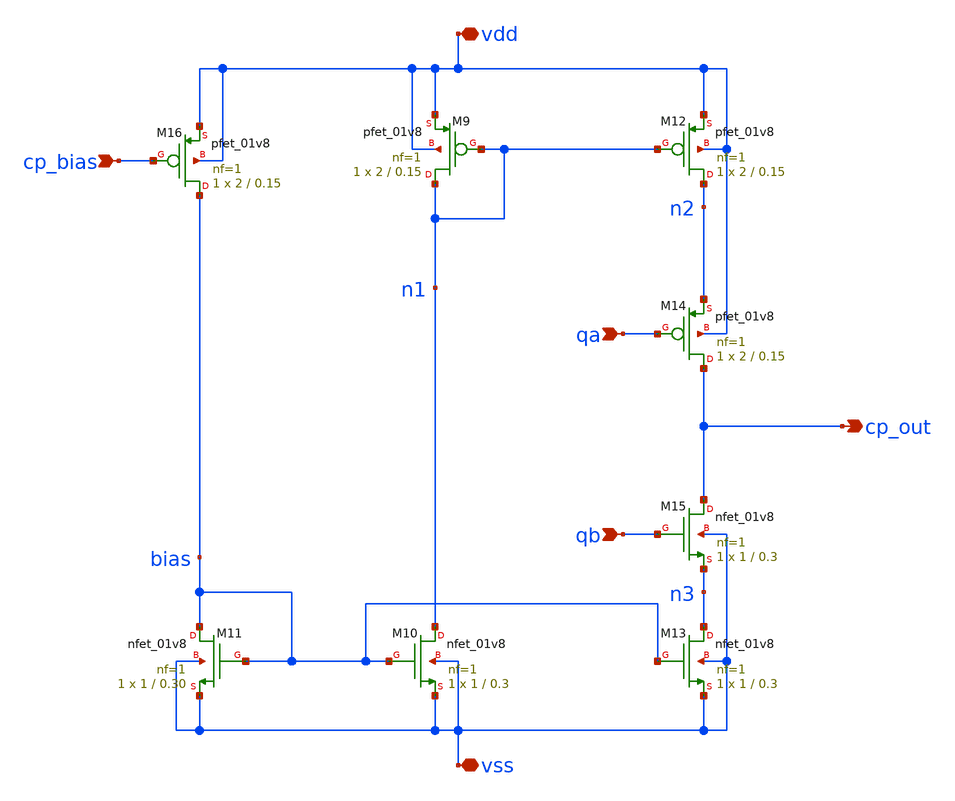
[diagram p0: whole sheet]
** sch_path: xschem/cp/cp_layout.sch
**.subckt cp_layout qa qb cp_out vdd vss cp_bias
*.ipin qa
*.ipin qb
*.opin cp_out
*.iopin vdd
*.iopin vss
*.ipin cp_bias
XM9 n1 n1 vdd vdd sky130_fd_pr__pfet_01v8 L=0.15 W=2 nf=1 ad='int((nf+1)/2) * W/nf * 0.29' as='int((nf+2)/2) * W/nf * 0.29'
+ pd='2*int((nf+1)/2) * (W/nf + 0.29)' ps='2*int((nf+2)/2) * (W/nf + 0.29)' nrd='0.29 / W' nrs='0.29 / W'
+ sa=0 sb=0 sd=0 mult=1 m=1
XM10 n1 bias vss vss sky130_fd_pr__nfet_01v8 L=0.3 W=1 nf=1 ad='int((nf+1)/2) * W/nf * 0.29' as='int((nf+2)/2) * W/nf * 0.29'
+ pd='2*int((nf+1)/2) * (W/nf + 0.29)' ps='2*int((nf+2)/2) * (W/nf + 0.29)' nrd='0.29 / W' nrs='0.29 / W'
+ sa=0 sb=0 sd=0 mult=1 m=1
XM11 bias bias vss vss sky130_fd_pr__nfet_01v8 L=0.30 W=1 nf=1 ad='int((nf+1)/2) * W/nf * 0.29' as='int((nf+2)/2) * W/nf * 0.29'
+ pd='2*int((nf+1)/2) * (W/nf + 0.29)' ps='2*int((nf+2)/2) * (W/nf + 0.29)' nrd='0.29 / W' nrs='0.29 / W'
+ sa=0 sb=0 sd=0 mult=1 m=1
XM12 n2 n1 vdd vdd sky130_fd_pr__pfet_01v8 L=0.15 W=2 nf=1 ad='int((nf+1)/2) * W/nf * 0.29' as='int((nf+2)/2) * W/nf * 0.29'
+ pd='2*int((nf+1)/2) * (W/nf + 0.29)' ps='2*int((nf+2)/2) * (W/nf + 0.29)' nrd='0.29 / W' nrs='0.29 / W'
+ sa=0 sb=0 sd=0 mult=1 m=1
XM13 n3 bias vss vss sky130_fd_pr__nfet_01v8 L=0.3 W=1 nf=1 ad='int((nf+1)/2) * W/nf * 0.29' as='int((nf+2)/2) * W/nf * 0.29'
+ pd='2*int((nf+1)/2) * (W/nf + 0.29)' ps='2*int((nf+2)/2) * (W/nf + 0.29)' nrd='0.29 / W' nrs='0.29 / W'
+ sa=0 sb=0 sd=0 mult=1 m=1
XM14 cp_out qa n2 vdd sky130_fd_pr__pfet_01v8 L=0.15 W=2 nf=1 ad='int((nf+1)/2) * W/nf * 0.29' as='int((nf+2)/2) * W/nf * 0.29'
+ pd='2*int((nf+1)/2) * (W/nf + 0.29)' ps='2*int((nf+2)/2) * (W/nf + 0.29)' nrd='0.29 / W' nrs='0.29 / W'
+ sa=0 sb=0 sd=0 mult=1 m=1
XM15 cp_out qb n3 vss sky130_fd_pr__nfet_01v8 L=0.3 W=1 nf=1 ad='int((nf+1)/2) * W/nf * 0.29' as='int((nf+2)/2) * W/nf * 0.29'
+ pd='2*int((nf+1)/2) * (W/nf + 0.29)' ps='2*int((nf+2)/2) * (W/nf + 0.29)' nrd='0.29 / W' nrs='0.29 / W'
+ sa=0 sb=0 sd=0 mult=1 m=1
XM16 bias cp_bias vdd vdd sky130_fd_pr__pfet_01v8 L=0.15 W=2 nf=1 ad='int((nf+1)/2) * W/nf * 0.29' as='int((nf+2)/2) * W/nf * 0.29'
+ pd='2*int((nf+1)/2) * (W/nf + 0.29)' ps='2*int((nf+2)/2) * (W/nf + 0.29)' nrd='0.29 / W' nrs='0.29 / W'
+ sa=0 sb=0 sd=0 mult=1 m=1
**.ends
.end
